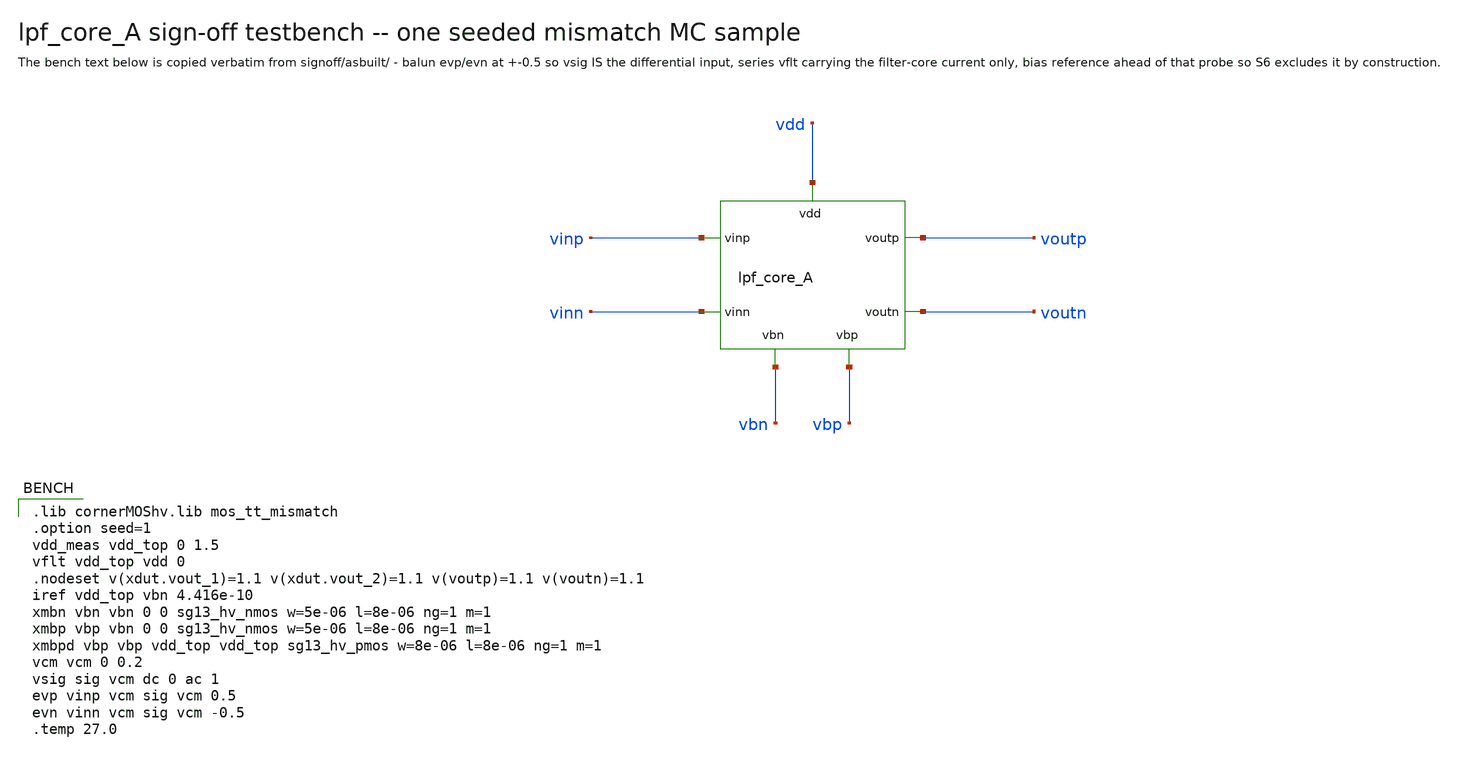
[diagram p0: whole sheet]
** sch_path: signoff/A-minarea/lpf_tb_A_mc.sch
**.subckt lpf_tb_A_mc
xdut vinp vinn voutp voutn vbn vbp vdd lpf_core_A
**** begin user architecture code

.lib cornerMOShv.lib mos_tt_mismatch
.option seed=1
vdd_meas vdd_top 0 1.5
vflt vdd_top vdd 0
.nodeset v(xdut.vout_1)=1.1 v(xdut.vout_2)=1.1 v(voutp)=1.1 v(voutn)=1.1
iref vdd_top vbn 4.416e-10
xmbn vbn vbn 0 0 sg13_hv_nmos w=5e-06 l=8e-06 ng=1 m=1
xmbp vbp vbn 0 0 sg13_hv_nmos w=5e-06 l=8e-06 ng=1 m=1
xmbpd vbp vbp vdd_top vdd_top sg13_hv_pmos w=8e-06 l=8e-06 ng=1 m=1
vcm vcm 0 0.2
vsig sig vcm dc 0 ac 1
evp vinp vcm sig vcm 0.5
evn vinn vcm sig vcm -0.5
.temp 27.0


.control
set filetype=binary
set appendwrite
op
write sim.raw
ac dec 50 0.1 1000
let hdiff = v(voutp) - v(voutn)
let hdb = db(mag(hdiff))
let dc_db = hdb[0]
let ph = cph(hdiff)
let gd = -deriv(ph) / (2 * pi)
let gd_dc_ms = gd[0] * 1e3
let gd_max_ms = vecmax(gd) * 1e3
let hrel = hdb - dc_db
meas ac fc_hz when hrel = -3 fall = 1
print dc_db gd_dc_ms gd_max_ms
write sim.raw hdiff ph gd frequency
.endc

**** end user architecture code
**.ends

* expanding   symbol:  lpf_core_A.sym # of pins=7
** sym_path: signoff/A-minarea/lpf_core_A.sym
** sch_path: signoff/A-minarea/lpf_core_A.sch
.subckt lpf_core_A vinp vinn voutp voutn vbn vbp vdd
*.ipin vinp
*.ipin vinn
*.opin voutp
*.opin voutn
*.ipin vdd
*.ipin vbn
*.ipin vbp
Xm2 net2 vinp vout_1 vout_1 sg13_hv_pmos w=8e-06 l=8e-06 ng=1 m=1 mm_ok=1
Xm5 net3 vinn vout_2 vout_2 sg13_hv_pmos w=8e-06 l=8e-06 ng=1 m=1 mm_ok=1
Xm4 vout_1 net2 0 0 sg13_hv_nmos w=4e-06 l=4e-06 ng=1 m=1 mm_ok=1
Xm8 vout_2 net3 0 0 sg13_hv_nmos w=4e-06 l=4e-06 ng=1 m=1 mm_ok=1
Xm9 net2 vbn 0 0 sg13_hv_nmos w=5e-06 l=8e-06 ng=1 m=1 mm_ok=1
Xm10 net3 vbn 0 0 sg13_hv_nmos w=5e-06 l=8e-06 ng=1 m=1 mm_ok=1
Xmst vout_1 vbn net4 net4 sg13_hv_pmos w=8.3e-07 l=8.4e-06 ng=1 m=1 mm_ok=1
Xmstn vout_2 vbn net1 net1 sg13_hv_pmos w=8.3e-07 l=8.4e-06 ng=1 m=1 mm_ok=1
Xm0 net4 vout_1 voutp voutp sg13_hv_pmos w=8e-06 l=8e-06 ng=1 m=1 mm_ok=1
Xm1 net1 vout_2 voutn voutn sg13_hv_pmos w=8e-06 l=8e-06 ng=1 m=1 mm_ok=1
Xm14 voutp net4 vdd vdd sg13_hv_pmos w=4.145e-06 l=1.2e-05 ng=1 m=1 mm_ok=1
Xm15 voutn net1 vdd vdd sg13_hv_pmos w=4.145e-06 l=1.2e-05 ng=1 m=1 mm_ok=1
c13 net2 vout_1 3.42107e-12 m=1
c17 net3 vout_2 3.42107e-12 m=1
c19 vout_2 vout_1 1.71624e-11 m=1
c1 voutp net4 3.34819e-11 m=1
c10 voutn net1 3.34819e-11 m=1
c12 voutn voutp 1.34455e-11 m=1
.ends

.end
